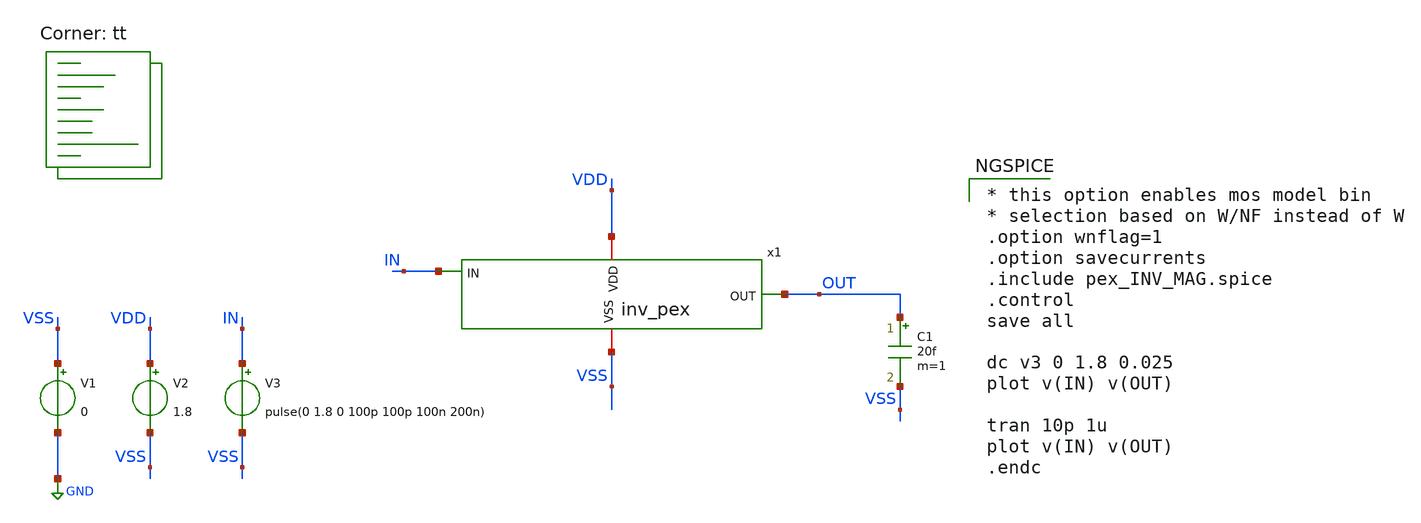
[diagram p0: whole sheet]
** sch_path: Xschem/inv _pex_tb.sch
**.subckt inv _pex_tb
V1 VSS GND 0
V2 VDD VSS 1.8
V3 IN VSS pulse(0 1.8 0 100p 100p 100n 200n)
C1 OUT VSS 20f m=1
x1 VSS VDD OUT IN inv_pex
**** begin user architecture code
.lib $::SKYWATER_MODELS/sky130.lib.spice tt

* this option enables mos model bin
* selection based on W/NF instead of W
.option wnflag=1
.option savecurrents
.include pex_INV_MAG.spice
.control
save all

dc v3 0 1.8 0.025
plot v(IN) v(OUT)

tran 10p 1u
plot v(IN) v(OUT)
.endc


**** end user architecture code
**.ends
.GLOBAL GND
.end
